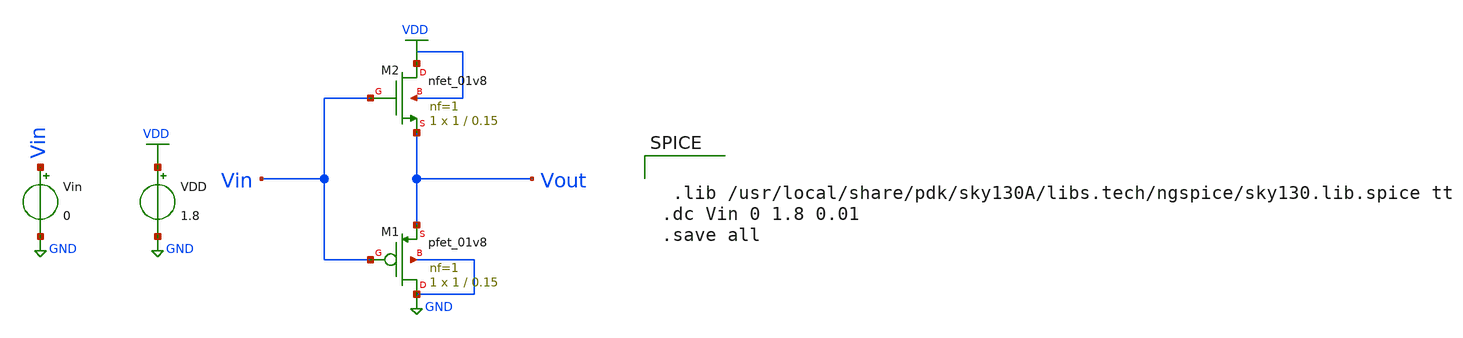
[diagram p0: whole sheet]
** sch_path: cmos_inv_ta.sch
**.subckt cmos_inv_ta
XM1 GND Vin Vout GND sky130_fd_pr__pfet_01v8 L=0.15 W=1 nf=1 ad='int((nf+1)/2) * W/nf * 0.29' as='int((nf+2)/2) * W/nf * 0.29'
+ pd='2*int((nf+1)/2) * (W/nf + 0.29)' ps='2*int((nf+2)/2) * (W/nf + 0.29)' nrd='0.29 / W' nrs='0.29 / W'
+ sa=0 sb=0 sd=0 mult=1 m=1
XM2 VDD Vin Vout VDD sky130_fd_pr__nfet_01v8 L=0.15 W=1 nf=1 ad='int((nf+1)/2) * W/nf * 0.29' as='int((nf+2)/2) * W/nf * 0.29'
+ pd='2*int((nf+1)/2) * (W/nf + 0.29)' ps='2*int((nf+2)/2) * (W/nf + 0.29)' nrd='0.29 / W' nrs='0.29 / W'
+ sa=0 sb=0 sd=0 mult=1 m=1
VDD VDD GND 1.8
Vin Vin GND 0
**** begin user architecture code


 .lib /usr/local/share/pdk/sky130A/libs.tech/ngspice/sky130.lib.spice tt
.dc Vin 0 1.8 0.01
.save all


** opencircuitdesign pdks install
.lib $::SKYWATER_MODELS/sky130.lib.spice tt


**** end user architecture code
**.ends
.GLOBAL VDD
.GLOBAL GND
.end
